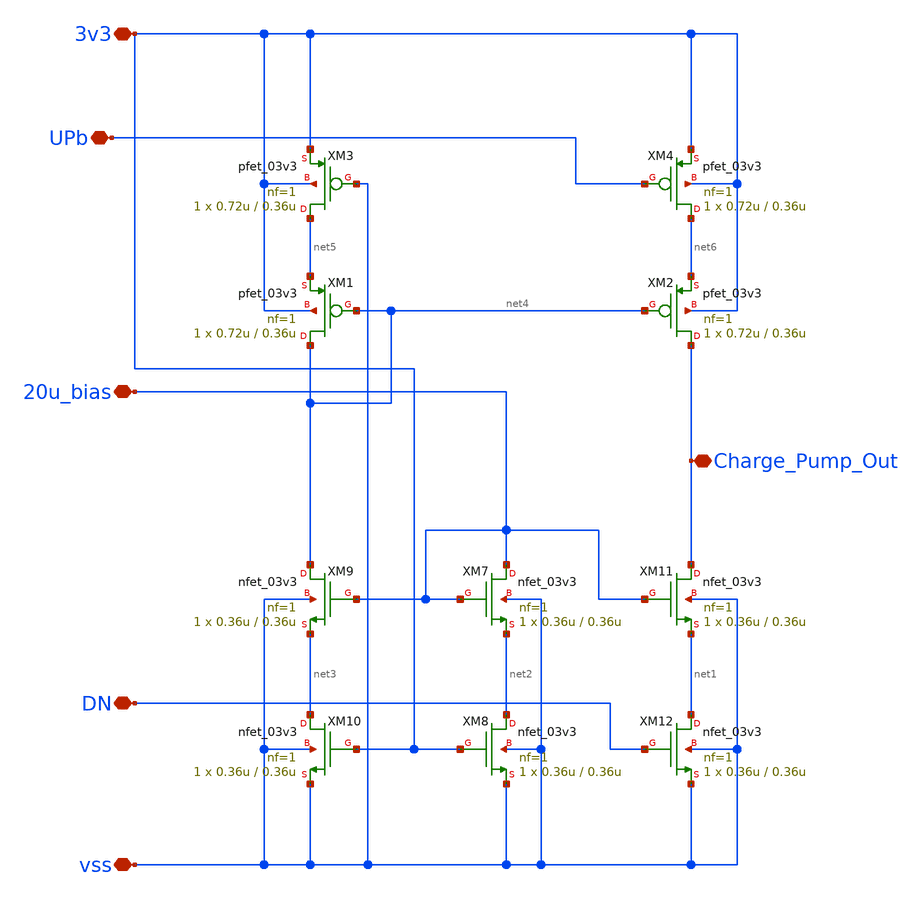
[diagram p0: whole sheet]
** sch_path: PLL/analog/schematics/Charge_Pump_FE_Block.sch
**.subckt Charge_Pump_FE_Block 3v3 vss 20u_bias UPb Charge_Pump_Out DN
*.iopin 3v3
*.iopin vss
*.iopin 20u_bias
*.iopin UPb
*.iopin Charge_Pump_Out
*.iopin DN
XM1 net4 net4 net5 3v3 pfet_03v3 L=0.36u W=0.72u nf=1 ad='int((nf+1)/2) * W/nf * 0.18u' as='int((nf+2)/2) * W/nf * 0.18u'
+ pd='2*int((nf+1)/2) * (W/nf + 0.18u)' ps='2*int((nf+2)/2) * (W/nf + 0.18u)' nrd='0.18u / W' nrs='0.18u / W'
+ sa=0 sb=0 sd=0 m=1
XM2 Charge_Pump_Out net4 net6 3v3 pfet_03v3 L=0.36u W=0.72u nf=1 ad='int((nf+1)/2) * W/nf * 0.18u' as='int((nf+2)/2) * W/nf * 0.18u'
+ pd='2*int((nf+1)/2) * (W/nf + 0.18u)' ps='2*int((nf+2)/2) * (W/nf + 0.18u)' nrd='0.18u / W' nrs='0.18u / W'
+ sa=0 sb=0 sd=0 m=1
XM3 net5 vss 3v3 3v3 pfet_03v3 L=0.36u W=0.72u nf=1 ad='int((nf+1)/2) * W/nf * 0.18u' as='int((nf+2)/2) * W/nf * 0.18u'
+ pd='2*int((nf+1)/2) * (W/nf + 0.18u)' ps='2*int((nf+2)/2) * (W/nf + 0.18u)' nrd='0.18u / W' nrs='0.18u / W'
+ sa=0 sb=0 sd=0 m=1
XM4 net6 UPb 3v3 3v3 pfet_03v3 L=0.36u W=0.72u nf=1 ad='int((nf+1)/2) * W/nf * 0.18u' as='int((nf+2)/2) * W/nf * 0.18u'
+ pd='2*int((nf+1)/2) * (W/nf + 0.18u)' ps='2*int((nf+2)/2) * (W/nf + 0.18u)' nrd='0.18u / W' nrs='0.18u / W'
+ sa=0 sb=0 sd=0 m=1
XM7 20u_bias 20u_bias net2 vss nfet_03v3 L=0.36u W=0.36u nf=1 ad='int((nf+1)/2) * W/nf * 0.18u' as='int((nf+2)/2) * W/nf * 0.18u'
+ pd='2*int((nf+1)/2) * (W/nf + 0.18u)' ps='2*int((nf+2)/2) * (W/nf + 0.18u)' nrd='0.18u / W' nrs='0.18u / W'
+ sa=0 sb=0 sd=0 m=1
XM8 net2 3v3 vss vss nfet_03v3 L=0.36u W=0.36u nf=1 ad='int((nf+1)/2) * W/nf * 0.18u' as='int((nf+2)/2) * W/nf * 0.18u'
+ pd='2*int((nf+1)/2) * (W/nf + 0.18u)' ps='2*int((nf+2)/2) * (W/nf + 0.18u)' nrd='0.18u / W' nrs='0.18u / W'
+ sa=0 sb=0 sd=0 m=1
XM9 net4 20u_bias net3 vss nfet_03v3 L=0.36u W=0.36u nf=1 ad='int((nf+1)/2) * W/nf * 0.18u' as='int((nf+2)/2) * W/nf * 0.18u'
+ pd='2*int((nf+1)/2) * (W/nf + 0.18u)' ps='2*int((nf+2)/2) * (W/nf + 0.18u)' nrd='0.18u / W' nrs='0.18u / W'
+ sa=0 sb=0 sd=0 m=1
XM10 net3 3v3 vss vss nfet_03v3 L=0.36u W=0.36u nf=1 ad='int((nf+1)/2) * W/nf * 0.18u' as='int((nf+2)/2) * W/nf * 0.18u'
+ pd='2*int((nf+1)/2) * (W/nf + 0.18u)' ps='2*int((nf+2)/2) * (W/nf + 0.18u)' nrd='0.18u / W' nrs='0.18u / W'
+ sa=0 sb=0 sd=0 m=1
XM11 Charge_Pump_Out 20u_bias net1 vss nfet_03v3 L=0.36u W=0.36u nf=1 ad='int((nf+1)/2) * W/nf * 0.18u'
+ as='int((nf+2)/2) * W/nf * 0.18u' pd='2*int((nf+1)/2) * (W/nf + 0.18u)' ps='2*int((nf+2)/2) * (W/nf + 0.18u)'
+ nrd='0.18u / W' nrs='0.18u / W' sa=0 sb=0 sd=0 m=1
XM12 net1 DN vss vss nfet_03v3 L=0.36u W=0.36u nf=1 ad='int((nf+1)/2) * W/nf * 0.18u' as='int((nf+2)/2) * W/nf * 0.18u'
+ pd='2*int((nf+1)/2) * (W/nf + 0.18u)' ps='2*int((nf+2)/2) * (W/nf + 0.18u)' nrd='0.18u / W' nrs='0.18u / W'
+ sa=0 sb=0 sd=0 m=1
**.ends
.end
